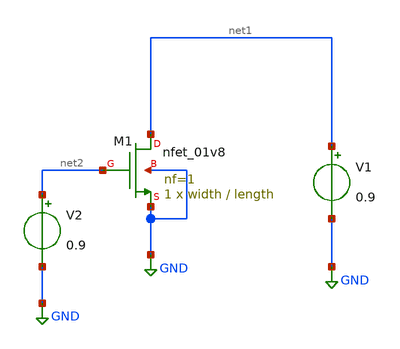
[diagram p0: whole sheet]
** sch_path: NMOS_Charac/nmos_gmid.sch
**.subckt nmos_gmid
V1 net1 GND 0.9
V2 net2 GND 0.9
XM1 net1 net2 GND GND sky130_fd_pr__nfet_01v8 L=length W=width nf=1 ad='int((nf+1)/2) * W/nf * 0.29'
+ as='int((nf+2)/2) * W/nf * 0.29' pd='2*int((nf+1)/2) * (W/nf + 0.29)' ps='2*int((nf+2)/2) * (W/nf + 0.29)'
+ nrd='0.29 / W' nrs='0.29 / W' sa=0 sb=0 sd=0 mult=1 m=1
**** begin user architecture code



.lib /usr/local/share/pdk/sky130A/libs.tech/ngspice/sky130.lib.spice tt
.option wnflag=1

.param length = 0.4
.param width = 1

.control
save all

save @m.xm1.msky130_fd_pr__nfet_01v8[gm]
save @m.xm1.msky130_fd_pr__nfet_01v8[id]
save @m.xm1.msky130_fd_pr__nfet_01v8[gds]
save @m.xm1.msky130_fd_pr__nfet_01v8[cgg]
save @m.xm1.msky130_fd_pr__nfet_01v8[vdsat]
save @m.xm1.msky130_fd_pr__nfet_01v8[vgs]

dc v2 0 1 1m

let gm = @m.xm1.msky130_fd_pr__nfet_01v8[gm]
let id = @m.xm1.msky130_fd_pr__nfet_01v8[id]
let gds = @m.xm1.msky130_fd_pr__nfet_01v8[gds]
let cgg = @m.xm1.msky130_fd_pr__nfet_01v8[cgg]
let vdsat = @m.xm1.msky130_fd_pr__nfet_01v8[vdsat]
let vgs = @m.xm1.msky130_fd_pr__nfet_01v8[vgs]

let gmro = gm/gds
let ft = gm/(2*pi*cgg)
let gmoverid = gm/id

wrdata gmro.txt gmro
wrdata ft.txt ft
wrdata gmoverid.txt gmoverid
wrdata id.txt id
wrdata vdsat.txt vdsat
wrdata vgs.txt vgs

.endc




**** end user architecture code
**.ends
.GLOBAL GND
.end
